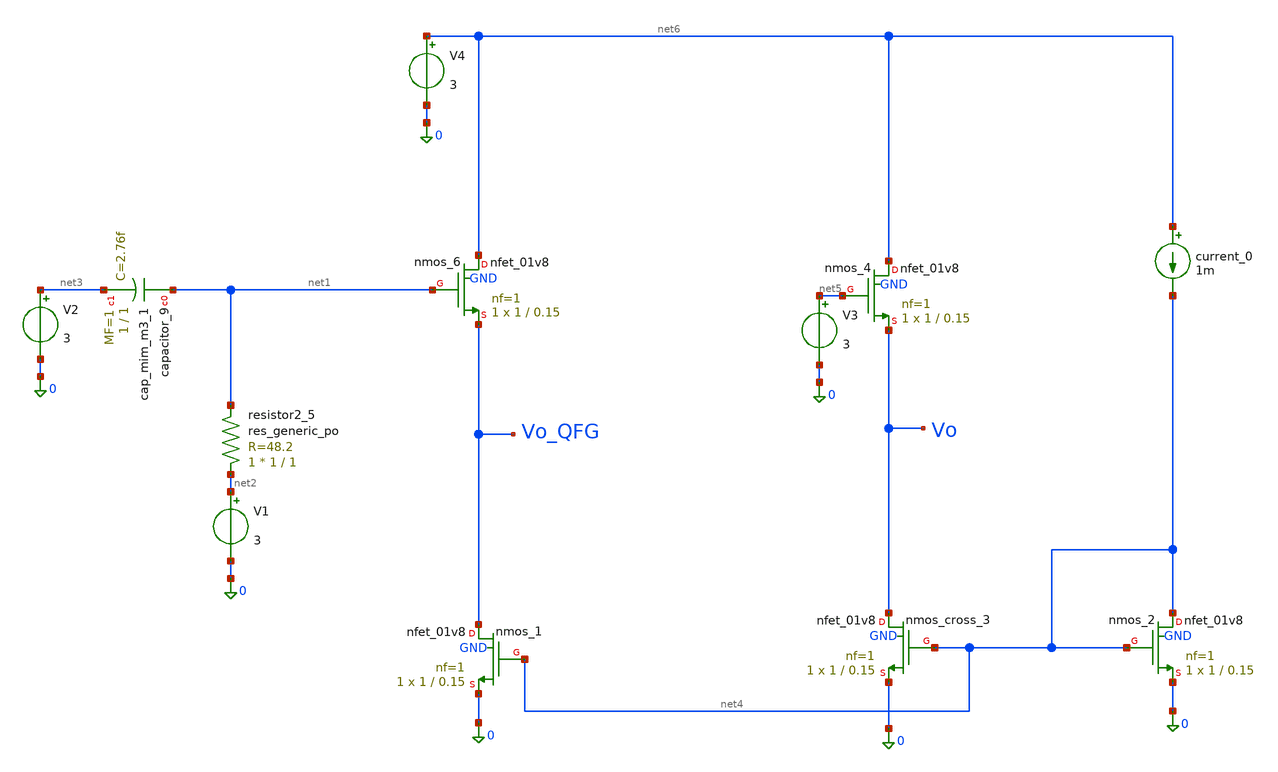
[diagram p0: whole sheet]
** sch_path: golden_netlists/10_1016_j_aeue_2023_154777_04_002.sch
**.subckt 10_1016_j_aeue_2023_154777_04_002
Xcapacitor_9 net1 net3 sky130_fd_pr__cap_mim_m3_1 W=1 L=1 MF=1 m=1
current_0 net6 net4 1m
Xnmos_1 Vo_QFG net4 0 GND sky130_fd_pr__nfet_01v8 L=0.15 W=1 nf=1 ad='int((nf+1)/2) * W/nf * 0.29' as='int((nf+2)/2) * W/nf * 0.29'
+ pd='2*int((nf+1)/2) * (W/nf + 0.29)' ps='2*int((nf+2)/2) * (W/nf + 0.29)' nrd='0.29 / W' nrs='0.29 / W'
+ sa=0 sb=0 sd=0 mult=1 m=1
Xnmos_2 net4 net4 0 GND sky130_fd_pr__nfet_01v8 L=0.15 W=1 nf=1 ad='int((nf+1)/2) * W/nf * 0.29' as='int((nf+2)/2) * W/nf * 0.29'
+ pd='2*int((nf+1)/2) * (W/nf + 0.29)' ps='2*int((nf+2)/2) * (W/nf + 0.29)' nrd='0.29 / W' nrs='0.29 / W'
+ sa=0 sb=0 sd=0 mult=1 m=1
Xnmos_4 net6 net5 Vo GND sky130_fd_pr__nfet_01v8 L=0.15 W=1 nf=1 ad='int((nf+1)/2) * W/nf * 0.29' as='int((nf+2)/2) * W/nf * 0.29'
+ pd='2*int((nf+1)/2) * (W/nf + 0.29)' ps='2*int((nf+2)/2) * (W/nf + 0.29)' nrd='0.29 / W' nrs='0.29 / W'
+ sa=0 sb=0 sd=0 mult=1 m=1
Xnmos_6 net6 net1 Vo_QFG GND sky130_fd_pr__nfet_01v8 L=0.15 W=1 nf=1 ad='int((nf+1)/2) * W/nf * 0.29'
+ as='int((nf+2)/2) * W/nf * 0.29' pd='2*int((nf+1)/2) * (W/nf + 0.29)' ps='2*int((nf+2)/2) * (W/nf + 0.29)'
+ nrd='0.29 / W' nrs='0.29 / W' sa=0 sb=0 sd=0 mult=1 m=1
Xnmos_cross_3 Vo net4 0 GND sky130_fd_pr__nfet_01v8 L=0.15 W=1 nf=1 ad='int((nf+1)/2) * W/nf * 0.29'
+ as='int((nf+2)/2) * W/nf * 0.29' pd='2*int((nf+1)/2) * (W/nf + 0.29)' ps='2*int((nf+2)/2) * (W/nf + 0.29)'
+ nrd='0.29 / W' nrs='0.29 / W' sa=0 sb=0 sd=0 mult=1 m=1
Xresistor2_5 net2 net1 sky130_fd_pr__res_generic_po W=1 L=1 m=1
V1 net2 0 3
V2 net3 0 3
V3 net5 0 3
V4 net6 0 3
**.ends
.end
